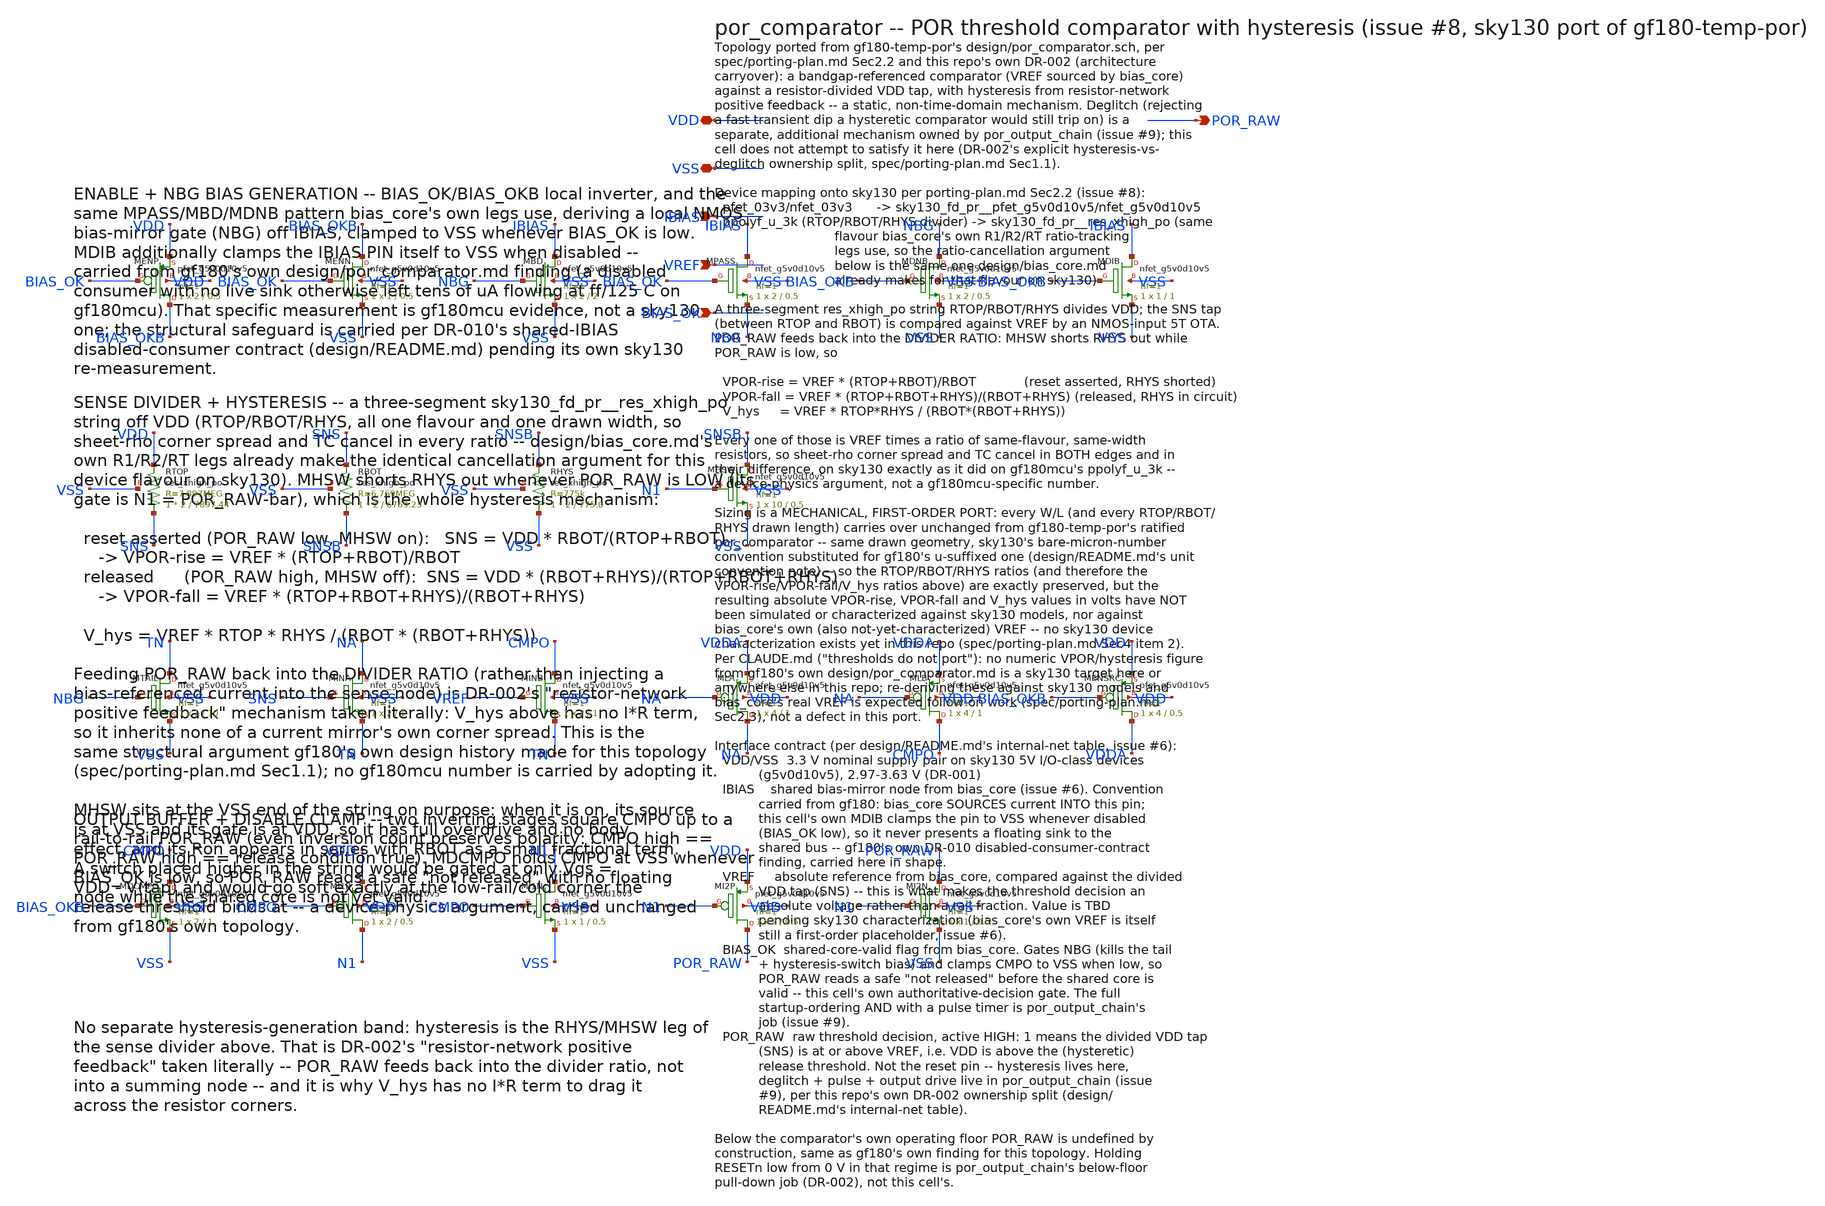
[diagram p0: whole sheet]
** sch_path: design/por_comparator.sch
**.subckt por_comparator VDD VSS IBIAS VREF BIAS_OK POR_RAW
*.iopin VDD
*.iopin VSS
*.ipin IBIAS
*.ipin VREF
*.ipin BIAS_OK
*.opin POR_RAW
XMENP BIAS_OKB BIAS_OK VDD VDD sky130_fd_pr__pfet_g5v0d10v5 L=0.5 W=2 nf=1 ad='int((1 + 1)/2) * 2 / 1 * 0.29'
+ as='int((1 + 2)/2) * 2 / 1 * 0.29' pd='2*int((1 + 1)/2) * (2 / 1 + 0.29)' ps='2*int((1 + 2)/2) * (2 / 1 + 0.29)'
+ nrd='0.29 / 2 ' nrs='0.29 / 2 ' sa=0 sb=0 sd=0 mult=1 m=1
XMENN BIAS_OKB BIAS_OK VSS VSS sky130_fd_pr__nfet_g5v0d10v5 L=0.5 W=1 nf=1 ad='int((1 + 1)/2) * 1 / 1 * 0.29'
+ as='int((1 + 2)/2) * 1 / 1 * 0.29' pd='2*int((1 + 1)/2) * (1 / 1 + 0.29)' ps='2*int((1 + 2)/2) * (1 / 1 + 0.29)'
+ nrd='0.29 / 1 ' nrs='0.29 / 1 ' sa=0 sb=0 sd=0 mult=1 m=1
XMBD IBIAS NBG VSS VSS sky130_fd_pr__nfet_g5v0d10v5 L=2 W=2 nf=1 ad='int((1 + 1)/2) * 2 / 1 * 0.29' as='int((1 + 2)/2) * 2 / 1 * 0.29'
+ pd='2*int((1 + 1)/2) * (2 / 1 + 0.29)' ps='2*int((1 + 2)/2) * (2 / 1 + 0.29)' nrd='0.29 / 2 ' nrs='0.29 / 2 '
+ sa=0 sb=0 sd=0 mult=1 m=1
XMPASS IBIAS BIAS_OK NBG VSS sky130_fd_pr__nfet_g5v0d10v5 L=0.5 W=2 nf=1 ad='int((1 + 1)/2) * 2 / 1 * 0.29'
+ as='int((1 + 2)/2) * 2 / 1 * 0.29' pd='2*int((1 + 1)/2) * (2 / 1 + 0.29)' ps='2*int((1 + 2)/2) * (2 / 1 + 0.29)'
+ nrd='0.29 / 2 ' nrs='0.29 / 2 ' sa=0 sb=0 sd=0 mult=1 m=1
XMDNB NBG BIAS_OKB VSS VSS sky130_fd_pr__nfet_g5v0d10v5 L=0.5 W=2 nf=1 ad='int((1 + 1)/2) * 2 / 1 * 0.29'
+ as='int((1 + 2)/2) * 2 / 1 * 0.29' pd='2*int((1 + 1)/2) * (2 / 1 + 0.29)' ps='2*int((1 + 2)/2) * (2 / 1 + 0.29)'
+ nrd='0.29 / 2 ' nrs='0.29 / 2 ' sa=0 sb=0 sd=0 mult=1 m=1
XMDIB IBIAS BIAS_OKB VSS VSS sky130_fd_pr__nfet_g5v0d10v5 L=1 W=1 nf=1 ad='int((1 + 1)/2) * 1 / 1 * 0.29'
+ as='int((1 + 2)/2) * 1 / 1 * 0.29' pd='2*int((1 + 1)/2) * (1 / 1 + 0.29)' ps='2*int((1 + 2)/2) * (1 / 1 + 0.29)'
+ nrd='0.29 / 1 ' nrs='0.29 / 1 ' sa=0 sb=0 sd=0 mult=1 m=1
XRTOP SNS VDD VSS sky130_fd_pr__res_xhigh_po W=2 L=7897.44 mult=1 m=1
XRBOT SNSB SNS VSS sky130_fd_pr__res_xhigh_po W=2 L=6769.23 mult=1 m=1
XRHYS VSS SNSB VSS sky130_fd_pr__res_xhigh_po W=2 L=775.0 mult=1 m=1
XMHSW SNSB N1 VSS VSS sky130_fd_pr__nfet_g5v0d10v5 L=0.5 W=10 nf=1 ad='int((1 + 1)/2) * 10 / 1 * 0.29'
+ as='int((1 + 2)/2) * 10 / 1 * 0.29' pd='2*int((1 + 1)/2) * (10 / 1 + 0.29)' ps='2*int((1 + 2)/2) * (10 / 1 + 0.29)'
+ nrd='0.29 / 10 ' nrs='0.29 / 10 ' sa=0 sb=0 sd=0 mult=1 m=1
XMTAIL TN NBG VSS VSS sky130_fd_pr__nfet_g5v0d10v5 L=10 W=1 nf=1 ad='int((1 + 1)/2) * 1 / 1 * 0.29' as='int((1 + 2)/2) * 1 / 1 * 0.29'
+ pd='2*int((1 + 1)/2) * (1 / 1 + 0.29)' ps='2*int((1 + 2)/2) * (1 / 1 + 0.29)' nrd='0.29 / 1 ' nrs='0.29 / 1 '
+ sa=0 sb=0 sd=0 mult=1 m=1
XMINA NA SNS TN VSS sky130_fd_pr__nfet_g5v0d10v5 L=1 W=2 nf=1 ad='int((1 + 1)/2) * 2 / 1 * 0.29' as='int((1 + 2)/2) * 2 / 1 * 0.29'
+ pd='2*int((1 + 1)/2) * (2 / 1 + 0.29)' ps='2*int((1 + 2)/2) * (2 / 1 + 0.29)' nrd='0.29 / 2 ' nrs='0.29 / 2 '
+ sa=0 sb=0 sd=0 mult=1 m=1
XMINB CMPO VREF TN VSS sky130_fd_pr__nfet_g5v0d10v5 L=1 W=2 nf=1 ad='int((1 + 1)/2) * 2 / 1 * 0.29' as='int((1 + 2)/2) * 2 / 1 * 0.29'
+ pd='2*int((1 + 1)/2) * (2 / 1 + 0.29)' ps='2*int((1 + 2)/2) * (2 / 1 + 0.29)' nrd='0.29 / 2 ' nrs='0.29 / 2 '
+ sa=0 sb=0 sd=0 mult=1 m=1
XMLA NA NA VDDA VDD sky130_fd_pr__pfet_g5v0d10v5 L=1 W=4 nf=1 ad='int((1 + 1)/2) * 4 / 1 * 0.29' as='int((1 + 2)/2) * 4 / 1 * 0.29'
+ pd='2*int((1 + 1)/2) * (4 / 1 + 0.29)' ps='2*int((1 + 2)/2) * (4 / 1 + 0.29)' nrd='0.29 / 4 ' nrs='0.29 / 4 '
+ sa=0 sb=0 sd=0 mult=1 m=1
XMLB CMPO NA VDDA VDD sky130_fd_pr__pfet_g5v0d10v5 L=1 W=4 nf=1 ad='int((1 + 1)/2) * 4 / 1 * 0.29' as='int((1 + 2)/2) * 4 / 1 * 0.29'
+ pd='2*int((1 + 1)/2) * (4 / 1 + 0.29)' ps='2*int((1 + 2)/2) * (4 / 1 + 0.29)' nrd='0.29 / 4 ' nrs='0.29 / 4 '
+ sa=0 sb=0 sd=0 mult=1 m=1
XMENSRC VDDA BIAS_OKB VDD VDD sky130_fd_pr__pfet_g5v0d10v5 L=0.5 W=4 nf=1 ad='int((1 + 1)/2) * 4 / 1 * 0.29'
+ as='int((1 + 2)/2) * 4 / 1 * 0.29' pd='2*int((1 + 1)/2) * (4 / 1 + 0.29)' ps='2*int((1 + 2)/2) * (4 / 1 + 0.29)'
+ nrd='0.29 / 4 ' nrs='0.29 / 4 ' sa=0 sb=0 sd=0 mult=1 m=1
XMDCMPO CMPO BIAS_OKB VSS VSS sky130_fd_pr__nfet_g5v0d10v5 L=1 W=2 nf=1 ad='int((1 + 1)/2) * 2 / 1 * 0.29'
+ as='int((1 + 2)/2) * 2 / 1 * 0.29' pd='2*int((1 + 1)/2) * (2 / 1 + 0.29)' ps='2*int((1 + 2)/2) * (2 / 1 + 0.29)'
+ nrd='0.29 / 2 ' nrs='0.29 / 2 ' sa=0 sb=0 sd=0 mult=1 m=1
XMI1P N1 CMPO VDD VDD sky130_fd_pr__pfet_g5v0d10v5 L=0.5 W=2 nf=1 ad='int((1 + 1)/2) * 2 / 1 * 0.29'
+ as='int((1 + 2)/2) * 2 / 1 * 0.29' pd='2*int((1 + 1)/2) * (2 / 1 + 0.29)' ps='2*int((1 + 2)/2) * (2 / 1 + 0.29)'
+ nrd='0.29 / 2 ' nrs='0.29 / 2 ' sa=0 sb=0 sd=0 mult=1 m=1
XMI1N N1 CMPO VSS VSS sky130_fd_pr__nfet_g5v0d10v5 L=0.5 W=1 nf=1 ad='int((1 + 1)/2) * 1 / 1 * 0.29'
+ as='int((1 + 2)/2) * 1 / 1 * 0.29' pd='2*int((1 + 1)/2) * (1 / 1 + 0.29)' ps='2*int((1 + 2)/2) * (1 / 1 + 0.29)'
+ nrd='0.29 / 1 ' nrs='0.29 / 1 ' sa=0 sb=0 sd=0 mult=1 m=1
XMI2P POR_RAW N1 VDD VDD sky130_fd_pr__pfet_g5v0d10v5 L=0.5 W=2 nf=1 ad='int((1 + 1)/2) * 2 / 1 * 0.29'
+ as='int((1 + 2)/2) * 2 / 1 * 0.29' pd='2*int((1 + 1)/2) * (2 / 1 + 0.29)' ps='2*int((1 + 2)/2) * (2 / 1 + 0.29)'
+ nrd='0.29 / 2 ' nrs='0.29 / 2 ' sa=0 sb=0 sd=0 mult=1 m=1
XMI2N POR_RAW N1 VSS VSS sky130_fd_pr__nfet_g5v0d10v5 L=0.5 W=1 nf=1 ad='int((1 + 1)/2) * 1 / 1 * 0.29'
+ as='int((1 + 2)/2) * 1 / 1 * 0.29' pd='2*int((1 + 1)/2) * (1 / 1 + 0.29)' ps='2*int((1 + 2)/2) * (1 / 1 + 0.29)'
+ nrd='0.29 / 1 ' nrs='0.29 / 1 ' sa=0 sb=0 sd=0 mult=1 m=1
**.ends
.end
